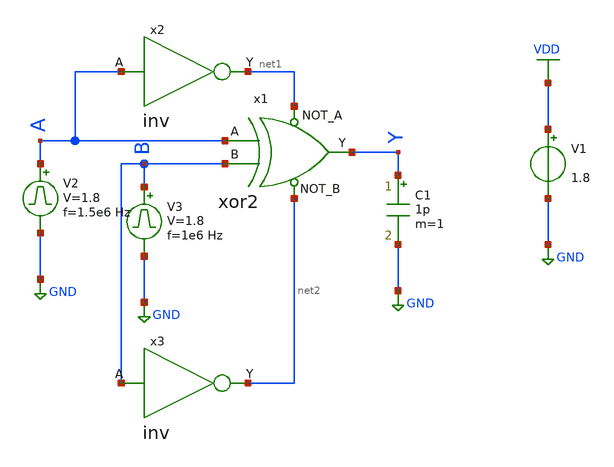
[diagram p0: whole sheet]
** sch_path: library/xschem/xor2_tb.sch
**.subckt xor2_tb
V1 VDD GND 1.8
V2 A GND pulse 0 1.8 '0.495/ 1.5e6 ' '0.01/1.5e6 ' '0.01/1.5e6 ' '0.49/1.5e6 ' '1/1.5e6 '
C1 Y GND 1p m=1
V3 B GND pulse 0 1.8 '0.495/ 1e6 ' '0.01/1e6 ' '0.01/1e6 ' '0.49/1e6 ' '1/1e6 '
x1 A B net1 net2 Y xor2
x2 A net1 inv
x3 B net2 inv
**** begin user architecture code


.control
save all
tran 1n 2u
plot V(A) V(B)+2 V(Y)+4
.endc


** opencircuitdesign pdks install
.lib $::SKYWATER_MODELS/sky130.lib.spice tt


**** end user architecture code
**.ends

* expanding   symbol:  xor2.sym # of pins=5
** sym_path: library/xschem/xor2.sym
** sch_path: library/xschem/xor2.sch
.subckt xor2 A B NOT_A NOT_B Y
*.opin Y
*.ipin A
*.ipin B
*.ipin NOT_A
*.ipin NOT_B
XM1 Y NOT_B net2 GND sky130_fd_pr__nfet_01v8 L=0.15 W=1 nf=1 ad='int((nf+1)/2) * W/nf * 0.29' as='int((nf+2)/2) * W/nf * 0.29'
+ pd='2*int((nf+1)/2) * (W/nf + 0.29)' ps='2*int((nf+2)/2) * (W/nf + 0.29)' nrd='0.29 / W' nrs='0.29 / W'
+ sa=0 sb=0 sd=0 mult=1 m=1
XM2 net1 A VDD VDD sky130_fd_pr__pfet_01v8 L=0.15 W=1 nf=1 ad='int((nf+1)/2) * W/nf * 0.29' as='int((nf+2)/2) * W/nf * 0.29'
+ pd='2*int((nf+1)/2) * (W/nf + 0.29)' ps='2*int((nf+2)/2) * (W/nf + 0.29)' nrd='0.29 / W' nrs='0.29 / W'
+ sa=0 sb=0 sd=0 mult=1 m=1
XM4 net2 NOT_A GND GND sky130_fd_pr__nfet_01v8 L=0.15 W=1 nf=1 ad='int((nf+1)/2) * W/nf * 0.29' as='int((nf+2)/2) * W/nf * 0.29'
+ pd='2*int((nf+1)/2) * (W/nf + 0.29)' ps='2*int((nf+2)/2) * (W/nf + 0.29)' nrd='0.29 / W' nrs='0.29 / W'
+ sa=0 sb=0 sd=0 mult=1 m=1
XM3 net1 B VDD VDD sky130_fd_pr__pfet_01v8 L=0.15 W=1 nf=1 ad='int((nf+1)/2) * W/nf * 0.29' as='int((nf+2)/2) * W/nf * 0.29'
+ pd='2*int((nf+1)/2) * (W/nf + 0.29)' ps='2*int((nf+2)/2) * (W/nf + 0.29)' nrd='0.29 / W' nrs='0.29 / W'
+ sa=0 sb=0 sd=0 mult=1 m=1
XM5 Y NOT_B net1 VDD sky130_fd_pr__pfet_01v8 L=0.15 W=1 nf=1 ad='int((nf+1)/2) * W/nf * 0.29' as='int((nf+2)/2) * W/nf * 0.29'
+ pd='2*int((nf+1)/2) * (W/nf + 0.29)' ps='2*int((nf+2)/2) * (W/nf + 0.29)' nrd='0.29 / W' nrs='0.29 / W'
+ sa=0 sb=0 sd=0 mult=1 m=1
XM6 Y NOT_A net1 VDD sky130_fd_pr__pfet_01v8 L=0.15 W=1 nf=1 ad='int((nf+1)/2) * W/nf * 0.29' as='int((nf+2)/2) * W/nf * 0.29'
+ pd='2*int((nf+1)/2) * (W/nf + 0.29)' ps='2*int((nf+2)/2) * (W/nf + 0.29)' nrd='0.29 / W' nrs='0.29 / W'
+ sa=0 sb=0 sd=0 mult=1 m=1
XM7 Y A net3 GND sky130_fd_pr__nfet_01v8 L=0.15 W=1 nf=1 ad='int((nf+1)/2) * W/nf * 0.29' as='int((nf+2)/2) * W/nf * 0.29'
+ pd='2*int((nf+1)/2) * (W/nf + 0.29)' ps='2*int((nf+2)/2) * (W/nf + 0.29)' nrd='0.29 / W' nrs='0.29 / W'
+ sa=0 sb=0 sd=0 mult=1 m=1
XM8 net3 B GND GND sky130_fd_pr__nfet_01v8 L=0.15 W=1 nf=1 ad='int((nf+1)/2) * W/nf * 0.29' as='int((nf+2)/2) * W/nf * 0.29'
+ pd='2*int((nf+1)/2) * (W/nf + 0.29)' ps='2*int((nf+2)/2) * (W/nf + 0.29)' nrd='0.29 / W' nrs='0.29 / W'
+ sa=0 sb=0 sd=0 mult=1 m=1
.ends


* expanding   symbol:  inv.sym # of pins=2
** sym_path: library/xschem/inv.sym
** sch_path: library/xschem/inv.sch
.subckt inv A Y
*.opin Y
*.ipin A
XM1 Y A GND GND sky130_fd_pr__nfet_01v8 L=0.15 W=1 nf=1 ad='int((nf+1)/2) * W/nf * 0.29' as='int((nf+2)/2) * W/nf * 0.29'
+ pd='2*int((nf+1)/2) * (W/nf + 0.29)' ps='2*int((nf+2)/2) * (W/nf + 0.29)' nrd='0.29 / W' nrs='0.29 / W'
+ sa=0 sb=0 sd=0 mult=1 m=1
XM2 Y A VDD VDD sky130_fd_pr__pfet_01v8 L=0.15 W=1 nf=1 ad='int((nf+1)/2) * W/nf * 0.29' as='int((nf+2)/2) * W/nf * 0.29'
+ pd='2*int((nf+1)/2) * (W/nf + 0.29)' ps='2*int((nf+2)/2) * (W/nf + 0.29)' nrd='0.29 / W' nrs='0.29 / W'
+ sa=0 sb=0 sd=0 mult=1 m=1
.ends

.GLOBAL VDD
.GLOBAL GND
.end
